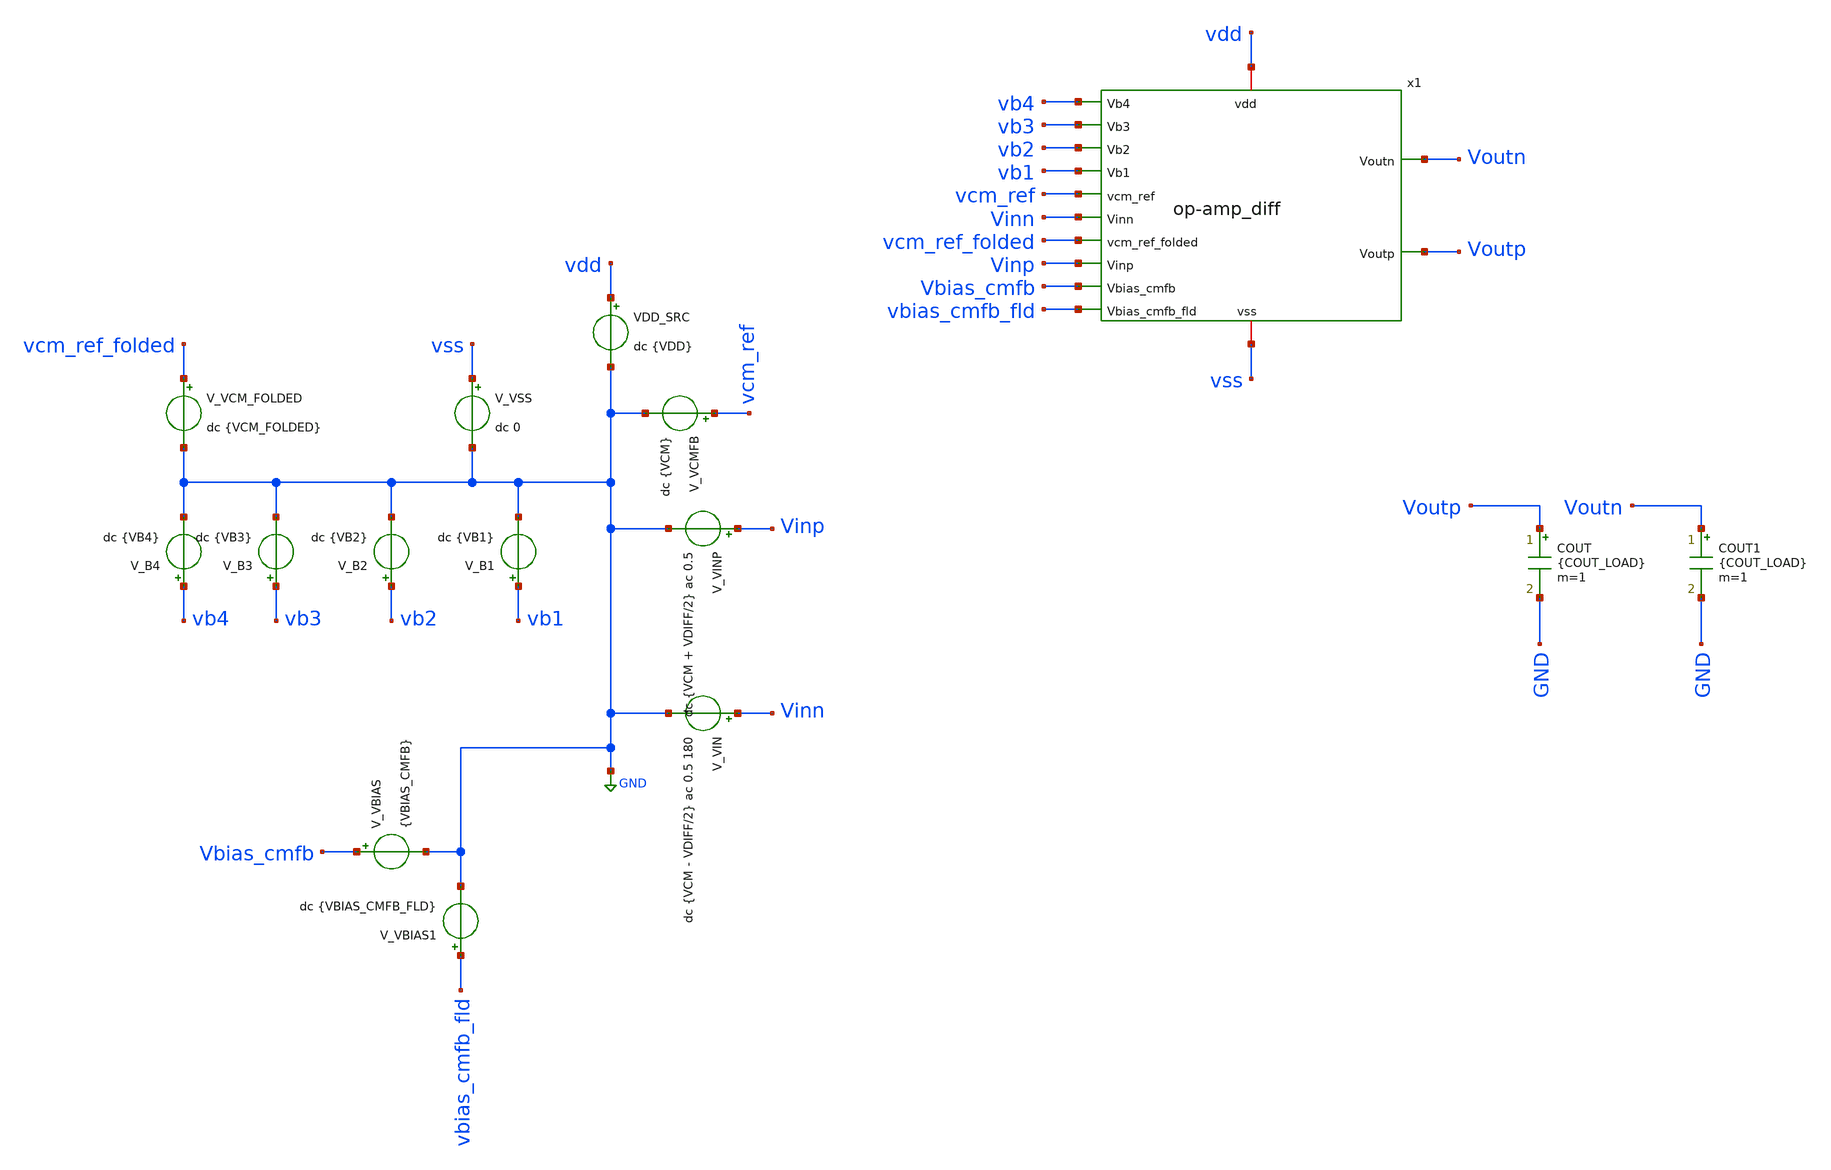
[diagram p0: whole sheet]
** sch_path: circuit_files/sar_adc_test/tb/ota_diff_tb.sch
**.subckt ota_diff_tb
V_VIN Vinn GND dc {VCM - VDIFF/2} ac 0.5 180
VDD_SRC vdd GND dc {VDD}
V_VINP Vinp GND dc {VCM + VDIFF/2} ac 0.5
V_VSS vss GND dc 0
V_VCMFB vcm_ref GND dc {VCM}
V_B1 vb1 GND dc {VB1}
V_B2 vb2 GND dc {VB2}
V_B3 vb3 GND dc {VB3}
V_B4 vb4 GND dc {VB4}
V_VCM_FOLDED vcm_ref_folded GND dc {VCM_FOLDED}
V_VBIAS Vbias_cmfb GND {VBIAS_CMFB}
V_VBIAS1 vbias_cmfb_fld GND dc {VBIAS_CMFB_FLD}
COUT Voutp GND {COUT_LOAD} m=1
COUT1 Voutn GND {COUT_LOAD} m=1
x1 vb4 vb3 vb2 vb1 Voutn vcm_ref Vinn Voutp vcm_ref_folded vdd Vinp vss Vbias_cmfb vbias_cmfb_fld
+ op-amp_diff
**** begin user architecture code

.include /foss/pdks/gf180mcuD/libs.tech/ngspice/design.ngspice

.lib /foss/pdks/gf180mcuD/libs.tech/ngspice/sm141064.ngspice typical
.lib /foss/pdks/gf180mcuD/libs.tech/ngspice/sm141064.ngspice res_typical
.lib /foss/pdks/gf180mcuD/libs.tech/ngspice/sm141064.ngspice moscap_typical
.lib /foss/pdks/gf180mcuD/libs.tech/ngspice/sm141064.ngspice diode_typical
.lib /foss/pdks/gf180mcuD/libs.tech/ngspice/sm141064.ngspice cap_mim
.lib /foss/pdks/gf180mcuD/libs.tech/ngspice/sm141064.ngspice mimcap_typical

.include /foss/pdks/gf180mcuD/libs.ref/gf180mcu_fd_io/spice/gf180mcu_fd_io.spice



.control

set noaskquit
set wr_singlescale
set measdgt=8
set numdgt=8
save all

shell rm -f ota_summary_report.txt
shell rm -f ota_detailed_report.txt
shell rm -f ota_ac_response.txt

echo ================================================== > ota_summary_report.txt
echo FINAL FULLY-DIFFERENTIAL OTA SUMMARY REPORT >> ota_summary_report.txt
echo NMOS-INPUT OTA WITH ACTIVE OUTPUT/FOLDED CMFB >> ota_summary_report.txt
echo ================================================== >> ota_summary_report.txt

echo ================================================== > ota_detailed_report.txt
echo FINAL FULLY-DIFFERENTIAL OTA DETAILED REPORT >> ota_detailed_report.txt
echo NMOS-INPUT OTA WITH ACTIVE OUTPUT/FOLDED CMFB >> ota_detailed_report.txt
echo ================================================== >> ota_detailed_report.txt

echo ---------------- PARAMETERS ---------------- >> ota_summary_report.txt
echo VDD=3.3 VCM=1.65 VDIFF=0 VCM_FOLDED=2.40 >> ota_summary_report.txt
echo VB1=0.58 VB2=2.637 VB3=2.25 VB4=1.15 >> ota_summary_report.txt
echo VBIAS_CMFB=0.82 VBIAS_CMFB_FLD=2.55 >> ota_summary_report.txt
echo Cn=500f Rn=8k COUT_LOAD=200f >> ota_summary_report.txt
echo Active output CMFB: no Rcm resistor network >> ota_summary_report.txt
echo Active folded CMFB: no Rcm_fld resistor network >> ota_summary_report.txt
echo CCMFB=500f CCMFB_FLD=1p >> ota_summary_report.txt
echo -------------------------------------------------- >> ota_summary_report.txt

echo ---------------- PARAMETERS ---------------- >> ota_detailed_report.txt
echo VDD=3.3 VCM=1.65 VDIFF=0 >> ota_detailed_report.txt
echo VCM_FOLDED=2.40 >> ota_detailed_report.txt
echo VB1=0.58 VB2=2.637 VB3=2.25 VB4=1.15 >> ota_detailed_report.txt
echo VBIAS_CMFB=0.82 VBIAS_CMFB_FLD=2.55 >> ota_detailed_report.txt
echo Cn=500f Rn=8k COUT_LOAD=200f >> ota_detailed_report.txt
echo Active output CMFB: no Rcm resistor network >> ota_detailed_report.txt
echo Active folded CMFB: no Rcm_fld resistor network >> ota_detailed_report.txt
echo CCMFB=500f CCMFB_FLD=1p >> ota_detailed_report.txt
echo -------------------------------------------------- >> ota_detailed_report.txt


* ============================================================
* DC OPERATING POINT
* ============================================================

op

let vdd_num          = 3.3

let voutcm_op        = 0.5*(v(voutp)+v(voutn))
let voutdiff_op      = v(voutp)-v(voutn)

let va_cm_op         = 0.5*(v(x1.va)+v(x1.vb))
let vx_cm_op         = 0.5*(v(x1.vx)+v(x1.vy))
let net45_cm_op      = 0.5*(v(x1.net4)+v(x1.net5))

let out_cm_err       = voutcm_op - v(vcm_ref)
let folded_cm_err    = va_cm_op - v(vcm_ref_folded)

let idd_op           = -i(VDD_SRC)
let pdc_op           = vdd_num*idd_op

echo ---------------- OP SUMMARY ---------------- >> ota_summary_report.txt
echo VOUTP VOUTN VOUTCM VOUTDIFF OUT_CM_ERR >> ota_summary_report.txt
echo $&v(voutp) $&v(voutn) $&voutcm_op $&voutdiff_op $&out_cm_err >> ota_summary_report.txt
echo VA VB VA_CM VCM_REF_FOLDED FOLDED_CM_ERR >> ota_summary_report.txt
echo $&v(x1.va) $&v(x1.vb) $&va_cm_op $&v(vcm_ref_folded) $&folded_cm_err >> ota_summary_report.txt
echo VBIAS_OUT VB5 NET8 NET9 IDD PDC >> ota_summary_report.txt
echo $&v(x1.vbias_out) $&v(x1.vb5) $&v(x1.net8) $&v(x1.net9) $&idd_op $&pdc_op >>
+ ota_summary_report.txt
echo -------------------------------------------------- >> ota_summary_report.txt

echo ---------------- OP DETAILED NODES ---------------- >> ota_detailed_report.txt
echo VOUTP=$&v(voutp) >> ota_detailed_report.txt
echo VOUTN=$&v(voutn) >> ota_detailed_report.txt
echo VOUTCM=$&voutcm_op >> ota_detailed_report.txt
echo VOUTDIFF=$&voutdiff_op >> ota_detailed_report.txt
echo VCM_REF_OUTPUT=$&v(vcm_ref) >> ota_detailed_report.txt
echo OUT_CM_ERR=$&out_cm_err >> ota_detailed_report.txt

echo VBIAS_OUT=$&v(x1.vbias_out) >> ota_detailed_report.txt

echo VX=$&v(x1.vx) >> ota_detailed_report.txt
echo VY=$&v(x1.vy) >> ota_detailed_report.txt
echo VX_CM=$&vx_cm_op >> ota_detailed_report.txt

echo VA=$&v(x1.va) >> ota_detailed_report.txt
echo VB=$&v(x1.vb) >> ota_detailed_report.txt
echo VA_CM=$&va_cm_op >> ota_detailed_report.txt
echo VCM_REF_FOLDED=$&v(vcm_ref_folded) >> ota_detailed_report.txt
echo FOLDED_CM_ERR=$&folded_cm_err >> ota_detailed_report.txt

echo NET1=$&v(x1.net1) >> ota_detailed_report.txt
echo NET4=$&v(x1.net4) >> ota_detailed_report.txt
echo NET5=$&v(x1.net5) >> ota_detailed_report.txt
echo NET4_NET5_CM=$&net45_cm_op >> ota_detailed_report.txt

echo VB5=$&v(x1.vb5) >> ota_detailed_report.txt
echo NET8=$&v(x1.net8) >> ota_detailed_report.txt
echo NET9=$&v(x1.net9) >> ota_detailed_report.txt

echo IDD=$&idd_op >> ota_detailed_report.txt
echo PDC=$&pdc_op >> ota_detailed_report.txt
echo -------------------------------------------------- >> ota_detailed_report.txt

print v(voutp) v(voutn) voutcm_op voutdiff_op out_cm_err
print v(x1.vbias_out)
print v(x1.vx) v(x1.vy) vx_cm_op
print v(x1.va) v(x1.vb) va_cm_op folded_cm_err
print v(x1.net1) v(x1.net4) v(x1.net5) net45_cm_op
print v(x1.vb5) v(x1.net8) v(x1.net9)
print idd_op pdc_op


* ============================================================
* DIFFERENTIAL AC ANALYSIS
*
* Input source setup expected:
*   V_VINP Vinp GND dc {VCM + VDIFF/2} ac 0.5
*   V_VIN  Vinn GND dc {VCM - VDIFF/2} ac 0.5 180
*
* This gives vin_diff = Vinp - Vinn = 1 V AC.
* ============================================================

ac dec 200 1 1G

let vin_diff        = v(vinp)-v(vinn)
let vin_cm          = 0.5*(v(vinp)+v(vinn))

let vin_diff_mag    = mag(vin_diff)
let vin_cm_mag      = mag(vin_cm)

let vout_diff       = v(voutp)-v(voutn)
let vout_cm_ac      = 0.5*(v(voutp)+v(voutn))

let vout_diff_mag   = mag(vout_diff)
let vout_cm_mag     = mag(vout_cm_ac)

let avd             = vout_diff/(vin_diff+1e-30)
let avd_mag         = mag(avd)
let avd_db          = 20*log10(avd_mag+1e-30)

let avd_phase_rad   = cph(avd)
let avd_phase_deg   = 57.2957795*avd_phase_rad

let gain_voutp      = v(voutp)/(vin_diff+1e-30)
let gain_voutn      = v(voutn)/(vin_diff+1e-30)
let gain_cmout      = vout_cm_ac/(vin_diff+1e-30)

let gain_voutp_db   = 20*log10(mag(gain_voutp)+1e-30)
let gain_voutn_db   = 20*log10(mag(gain_voutn)+1e-30)
let gain_cmout_db   = 20*log10(mag(gain_cmout)+1e-30)

* Differential-input to output-common-mode leakage.
* This should be as negative as possible.
let cm_leak_ratio   = vout_cm_ac/(vout_diff+1e-30)
let cm_leak_rel_db  = 20*log10(mag(cm_leak_ratio)+1e-30)

* Same information but positive number:
* AVD_DB - GAIN_CMOUT_DB.
let cm_rej_from_diff_db = avd_db - gain_cmout_db

let gain_vxvy       = (v(x1.vx)-v(x1.vy))/(vin_diff+1e-30)
let gain_vavb       = (v(x1.va)-v(x1.vb))/(vin_diff+1e-30)
let gain_stage2     = avd/(gain_vavb+1e-30)

let gain_vxvy_db    = 20*log10(mag(gain_vxvy)+1e-30)
let gain_vavb_db    = 20*log10(mag(gain_vavb)+1e-30)
let gain_stage2_db  = 20*log10(mag(gain_stage2)+1e-30)

let gain_vx_db      = 20*log10(mag(v(x1.vx)/(vin_diff+1e-30))+1e-30)
let gain_vy_db      = 20*log10(mag(v(x1.vy)/(vin_diff+1e-30))+1e-30)
let gain_va_db      = 20*log10(mag(v(x1.va)/(vin_diff+1e-30))+1e-30)
let gain_vb_db      = 20*log10(mag(v(x1.vb)/(vin_diff+1e-30))+1e-30)
let gain_net4_db    = 20*log10(mag(v(x1.net4)/(vin_diff+1e-30))+1e-30)
let gain_net5_db    = 20*log10(mag(v(x1.net5)/(vin_diff+1e-30))+1e-30)


* ============================================================
* LOW-FREQUENCY AC MEASUREMENTS
* ============================================================

meas ac VIN_DIFF_1HZ              find vin_diff_mag          at=1
meas ac VIN_CM_1HZ                find vin_cm_mag            at=1

meas ac VOUT_DIFF_MAG_1HZ         find vout_diff_mag         at=1
meas ac VOUT_CM_MAG_1HZ           find vout_cm_mag           at=1

meas ac AVD_MAG_1HZ               find avd_mag               at=1
meas ac AVD_DB_1HZ                find avd_db                at=1
meas ac AVD_PHASE_1HZ_RAD         find avd_phase_rad         at=1
meas ac AVD_PHASE_1HZ_DEG         find avd_phase_deg         at=1

meas ac GAIN_VOUTP_DB_1HZ         find gain_voutp_db         at=1
meas ac GAIN_VOUTN_DB_1HZ         find gain_voutn_db         at=1
meas ac GAIN_CMOUT_DB_1HZ         find gain_cmout_db         at=1

meas ac CM_LEAK_REL_DB_1HZ        find cm_leak_rel_db        at=1
meas ac CM_REJ_FROM_DIFF_DB_1HZ   find cm_rej_from_diff_db   at=1

meas ac GAIN_VX_DB_1HZ            find gain_vx_db            at=1
meas ac GAIN_VY_DB_1HZ            find gain_vy_db            at=1
meas ac GAIN_VA_DB_1HZ            find gain_va_db            at=1
meas ac GAIN_VB_DB_1HZ            find gain_vb_db            at=1
meas ac GAIN_NET4_DB_1HZ          find gain_net4_db          at=1
meas ac GAIN_NET5_DB_1HZ          find gain_net5_db          at=1

meas ac GAIN_VXVY_DB_1HZ          find gain_vxvy_db          at=1
meas ac GAIN_VAVB_DB_1HZ          find gain_vavb_db          at=1
meas ac GAIN_STAGE2_DB_1HZ        find gain_stage2_db        at=1


* ============================================================
* BANDWIDTH, UGF, PHASE MARGIN
* ============================================================

let avd_3db_target = avd_db_1hz - 3

meas ac FP_DOM                when avd_db=avd_3db_target fall=1
meas ac UGF                   when avd_db=0 fall=1
meas ac PHASE_AT_UGF_RAD      find avd_phase_rad when avd_db=0 fall=1
meas ac PHASE_AT_UGF_DEG      find avd_phase_deg when avd_db=0 fall=1

let phase_at_ugf_deg_wrapped = phase_at_ugf_deg

while phase_at_ugf_deg_wrapped < -180
  let phase_at_ugf_deg_wrapped = phase_at_ugf_deg_wrapped + 360
end

while phase_at_ugf_deg_wrapped > 180
  let phase_at_ugf_deg_wrapped = phase_at_ugf_deg_wrapped - 360
end

let PM_EST = 180 + phase_at_ugf_deg_wrapped


* ============================================================
* SPOT CHECKS
* ============================================================

meas ac AVD_DB_10K              find avd_db              at=10k
meas ac AVD_DB_100K             find avd_db              at=100k
meas ac AVD_DB_1MEG             find avd_db              at=1Meg
meas ac AVD_DB_10MEG            find avd_db              at=10Meg
meas ac AVD_DB_100MEG           find avd_db              at=100Meg

meas ac PHASE_10K_DEG           find avd_phase_deg       at=10k
meas ac PHASE_100K_DEG          find avd_phase_deg       at=100k
meas ac PHASE_1MEG_DEG          find avd_phase_deg       at=1Meg
meas ac PHASE_10MEG_DEG         find avd_phase_deg       at=10Meg
meas ac PHASE_100MEG_DEG        find avd_phase_deg       at=100Meg

meas ac GAIN_CMOUT_DB_10K       find gain_cmout_db       at=10k
meas ac GAIN_CMOUT_DB_100K      find gain_cmout_db       at=100k
meas ac GAIN_CMOUT_DB_1MEG      find gain_cmout_db       at=1Meg

meas ac CM_LEAK_REL_DB_10K      find cm_leak_rel_db      at=10k
meas ac CM_LEAK_REL_DB_100K     find cm_leak_rel_db      at=100k
meas ac CM_LEAK_REL_DB_1MEG     find cm_leak_rel_db      at=1Meg


* ============================================================
* WRITE SUMMARY REPORT
* ============================================================

echo ---------------- AC SUMMARY ---------------- >> ota_summary_report.txt
echo VIN_DIFF_1HZ=$&vin_diff_1hz >> ota_summary_report.txt
echo VIN_CM_1HZ=$&vin_cm_1hz >> ota_summary_report.txt
echo VOUT_DIFF_MAG_1HZ=$&vout_diff_mag_1hz >> ota_summary_report.txt
echo VOUT_CM_MAG_1HZ=$&vout_cm_mag_1hz >> ota_summary_report.txt

echo DC_DIFF_GAIN_LINEAR=$&avd_mag_1hz >> ota_summary_report.txt
echo DC_DIFF_GAIN_DB=$&avd_db_1hz >> ota_summary_report.txt
echo DC_PHASE_1HZ_DEG=$&avd_phase_1hz_deg >> ota_summary_report.txt

echo OUTPUT_CM_GAIN_FROM_DIFF_DB_1HZ=$&gain_cmout_db_1hz >> ota_summary_report.txt
echo OUTPUT_CM_LEAK_REL_TO_DIFF_DB_1HZ=$&cm_leak_rel_db_1hz >> ota_summary_report.txt
echo OUTPUT_CM_REJECTION_FROM_DIFF_DB_1HZ=$&cm_rej_from_diff_db_1hz >> ota_summary_report.txt

echo STAGE1_GAIN_VAVB_DB=$&gain_vavb_db_1hz >> ota_summary_report.txt
echo STAGE2_GAIN_EST_DB=$&gain_stage2_db_1hz >> ota_summary_report.txt

echo DOMINANT_POLE_HZ=$&fp_dom >> ota_summary_report.txt
echo UNITY_GAIN_FREQ_HZ=$&ugf >> ota_summary_report.txt
echo PHASE_AT_UGF_RAW_DEG=$&phase_at_ugf_deg >> ota_summary_report.txt
echo PHASE_AT_UGF_WRAPPED_DEG=$&phase_at_ugf_deg_wrapped >> ota_summary_report.txt
echo PHASE_MARGIN_EST_DEG=$&PM_EST >> ota_summary_report.txt
echo -------------------------------------------------- >> ota_summary_report.txt

echo ---------------- PASS TARGETS TO CHECK ---------------- >> ota_summary_report.txt
echo DC output CM: VOUTCM should be near 1.65 V >> ota_summary_report.txt
echo DC folded CM: VA_CM should be near 2.40 V >> ota_summary_report.txt
echo IDD target: roughly 100 uA to 300 uA is reasonable >> ota_summary_report.txt
echo Differential gain target: AVD_DB should be greater than 75 dB before layout >>
+ ota_summary_report.txt
echo Differential PM target: PM_EST should be greater than 60 deg >> ota_summary_report.txt
echo Output CM leakage target: CM_LEAK_REL_DB should be very negative, preferably below -50 dB >>
+ ota_summary_report.txt
echo Note: active MOS CMFB can create differential-to-common-mode leakage, so check this value
+ carefully. >> ota_summary_report.txt
echo ================================================== >> ota_summary_report.txt


* ============================================================
* WRITE DETAILED REPORT
* ============================================================

echo ---------------- AC DETAILED LOW-FREQUENCY GAINS ---------------- >> ota_detailed_report.txt
echo VIN_DIFF_1HZ=$&vin_diff_1hz >> ota_detailed_report.txt
echo VIN_CM_1HZ=$&vin_cm_1hz >> ota_detailed_report.txt

echo VOUT_DIFF_MAG_1HZ=$&vout_diff_mag_1hz >> ota_detailed_report.txt
echo VOUT_CM_MAG_1HZ=$&vout_cm_mag_1hz >> ota_detailed_report.txt

echo AVD_MAG_1HZ=$&avd_mag_1hz >> ota_detailed_report.txt
echo AVD_DB_1HZ=$&avd_db_1hz >> ota_detailed_report.txt
echo AVD_PHASE_1HZ_RAD=$&avd_phase_1hz_rad >> ota_detailed_report.txt
echo AVD_PHASE_1HZ_DEG=$&avd_phase_1hz_deg >> ota_detailed_report.txt

echo GAIN_VOUTP_DB_1HZ=$&gain_voutp_db_1hz >> ota_detailed_report.txt
echo GAIN_VOUTN_DB_1HZ=$&gain_voutn_db_1hz >> ota_detailed_report.txt
echo GAIN_CMOUT_DB_1HZ=$&gain_cmout_db_1hz >> ota_detailed_report.txt
echo CM_LEAK_REL_DB_1HZ=$&cm_leak_rel_db_1hz >> ota_detailed_report.txt
echo CM_REJ_FROM_DIFF_DB_1HZ=$&cm_rej_from_diff_db_1hz >> ota_detailed_report.txt

echo GAIN_VX_DB_1HZ=$&gain_vx_db_1hz >> ota_detailed_report.txt
echo GAIN_VY_DB_1HZ=$&gain_vy_db_1hz >> ota_detailed_report.txt
echo GAIN_VA_DB_1HZ=$&gain_va_db_1hz >> ota_detailed_report.txt
echo GAIN_VB_DB_1HZ=$&gain_vb_db_1hz >> ota_detailed_report.txt
echo GAIN_NET4_DB_1HZ=$&gain_net4_db_1hz >> ota_detailed_report.txt
echo GAIN_NET5_DB_1HZ=$&gain_net5_db_1hz >> ota_detailed_report.txt

echo GAIN_VXVY_DB_1HZ=$&gain_vxvy_db_1hz >> ota_detailed_report.txt
echo GAIN_VAVB_DB_1HZ=$&gain_vavb_db_1hz >> ota_detailed_report.txt
echo GAIN_STAGE2_DB_1HZ=$&gain_stage2_db_1hz >> ota_detailed_report.txt
echo -------------------------------------------------- >> ota_detailed_report.txt

echo ---------------- AC BANDWIDTH AND PHASE ---------------- >> ota_detailed_report.txt
echo AVD_3DB_TARGET=$&avd_3db_target >> ota_detailed_report.txt
echo FP_DOM_HZ=$&fp_dom >> ota_detailed_report.txt
echo UGF_HZ=$&ugf >> ota_detailed_report.txt
echo PHASE_AT_UGF_RAD=$&phase_at_ugf_rad >> ota_detailed_report.txt
echo PHASE_AT_UGF_RAW_DEG=$&phase_at_ugf_deg >> ota_detailed_report.txt
echo PHASE_AT_UGF_WRAPPED_DEG=$&phase_at_ugf_deg_wrapped >> ota_detailed_report.txt
echo PHASE_MARGIN_EST_DEG=$&PM_EST >> ota_detailed_report.txt

echo AVD_DB_10K=$&avd_db_10k PHASE_10K_DEG=$&phase_10k_deg >> ota_detailed_report.txt
echo AVD_DB_100K=$&avd_db_100k PHASE_100K_DEG=$&phase_100k_deg >> ota_detailed_report.txt
echo AVD_DB_1MEG=$&avd_db_1meg PHASE_1MEG_DEG=$&phase_1meg_deg >> ota_detailed_report.txt
echo AVD_DB_10MEG=$&avd_db_10meg PHASE_10MEG_DEG=$&phase_10meg_deg >> ota_detailed_report.txt
echo AVD_DB_100MEG=$&avd_db_100meg PHASE_100MEG_DEG=$&phase_100meg_deg >> ota_detailed_report.txt

echo GAIN_CMOUT_DB_10K=$&gain_cmout_db_10k CM_LEAK_REL_DB_10K=$&cm_leak_rel_db_10k >>
+ ota_detailed_report.txt
echo GAIN_CMOUT_DB_100K=$&gain_cmout_db_100k CM_LEAK_REL_DB_100K=$&cm_leak_rel_db_100k >>
+ ota_detailed_report.txt
echo GAIN_CMOUT_DB_1MEG=$&gain_cmout_db_1meg CM_LEAK_REL_DB_1MEG=$&cm_leak_rel_db_1meg >>
+ ota_detailed_report.txt
echo -------------------------------------------------- >> ota_detailed_report.txt

echo ---------------- INTERPRETATION NOTES ---------------- >> ota_detailed_report.txt
echo 1. VOUTCM should be near vcm_ref = 1.65 V. >> ota_detailed_report.txt
echo 2. VA_CM should be near vcm_ref_folded = 2.40 V. >> ota_detailed_report.txt
echo 3. VBIAS_OUT around 0.6 to 1.2 V is usually reasonable here. >> ota_detailed_report.txt
echo 4. VB5 around 0.5 to 0.9 V is usually reasonable here. >> ota_detailed_report.txt
echo 5. IDD should remain around hundreds of uA, not mA. >> ota_detailed_report.txt
echo 6. CM_LEAK_REL_DB is output common-mode divided by differential output under differential
+ drive. More negative is better. >> ota_detailed_report.txt
echo 7. This is pre-layout. Recheck after corners, mismatch, PEX, and CMFB loop-gain tests. >>
+ ota_detailed_report.txt
echo ================================================== >> ota_detailed_report.txt


* ============================================================
* SAVE FULL AC TABLE
* ============================================================

wrdata ota_ac_response.txt avd_db avd_phase_deg gain_vavb_db gain_stage2_db gain_cmout_db
+ cm_leak_rel_db cm_rej_from_diff_db gain_voutp_db gain_voutn_db


* ============================================================
* PRINT IMPORTANT VALUES TO TERMINAL
* ============================================================

print avd_mag_1hz avd_db_1hz gain_vavb_db_1hz gain_stage2_db_1hz
print vout_diff_mag_1hz vout_cm_mag_1hz gain_cmout_db_1hz cm_leak_rel_db_1hz cm_rej_from_diff_db_1hz
print fp_dom ugf phase_at_ugf_deg phase_at_ugf_deg_wrapped PM_EST
print avd_db_10k avd_db_100k avd_db_1meg avd_db_10meg avd_db_100meg
print gain_cmout_db_10k gain_cmout_db_100k gain_cmout_db_1meg
print cm_leak_rel_db_10k cm_leak_rel_db_100k cm_leak_rel_db_1meg

echo ==================================================
echo Done.
echo Generated:
echo   ota_summary_report.txt
echo   ota_detailed_report.txt
echo   ota_ac_response.txt
echo ==================================================

.endc





**** begin user architecture code

.param sw_stat_mismatch=0
.param mis_vth=0
.param mis_k=0

.param VDD=3.3
.param VCM=1.65
.param VCM_FOLDED=2.40
.param VDIFF=0

* ============================================================
* Final selected OTA bias
* ============================================================
.param VB1=0.58
.param VB2=2.637
.param VB3=2.25
.param VB4=1.15

.param VBIAS_CMFB=0.82
.param VBIAS_CMFB_FLD=2.55

* ============================================================
* Compensation / load
* ============================================================
.param Cn=500f
.param Rn=8k
.param COUT_LOAD=200f


.param CCMFB=500f
.param CCMFB_FLD=1p

.options reltol=1e-4 abstol=1e-12 vntol=1e-6
.options gmin=1e-12
.options plotwinsize=0
.options method=gear maxord=2

* ============================================================
* Operating-point hints only. These do not force final OP.
* Internal OTA nodes are now inside instance x1.
* ============================================================
.nodeset V(voutp)=1.643
.nodeset V(voutn)=1.643

.nodeset V(x1.vbias_out)=0.866

.nodeset V(x1.vx)=3.022
.nodeset V(x1.vy)=3.022
.nodeset V(x1.va)=2.401
.nodeset V(x1.vb)=2.401

.nodeset V(x1.net1)=0.887
.nodeset V(x1.net4)=0.426
.nodeset V(x1.net5)=0.426

.nodeset V(x1.vb5)=0.713
.nodeset V(x1.net8)=0.578
.nodeset V(x1.net9)=2.624



**** end user architecture code
**.ends

* expanding   symbol:  /media/sf_LNA_chipathon/sar_adc_gf180/xschem/op-amp_diff.sym # of pins=14
** sym_path: circuit_files/sar_adc_test/xschem/op-amp_diff.sym
** sch_path: circuit_files/sar_adc_test/xschem/op-amp_diff.sch
.subckt op-amp_diff Vb4 Vb3 Vb2 Vb1 Voutn vcm_ref Vinn Voutp vcm_ref_folded vdd Vinp vss Vbias_cmfb
+ Vbias_cmfb_fld
*.ipin Vinn
*.opin Voutp
*.iopin vdd
*.ipin Vinp
*.ipin Vb1
*.ipin Vbias_cmfb_fld
*.iopin vss
*.opin Voutn
*.ipin Vbias_cmfb
*.ipin Vb2
*.ipin Vb3
*.ipin Vb4
*.ipin vcm_ref_folded
*.ipin vcm_ref
XM1 Vy Vinn net1 vss nfet_03v3 L=0.5u W=20u nf=1 ad='int((nf+1)/2) * W/nf * 0.18u' as='int((nf+2)/2) * W/nf * 0.18u'
+ pd='2*int((nf+1)/2) * (W/nf + 0.18u)' ps='2*int((nf+2)/2) * (W/nf + 0.18u)' nrd='0.18u / W' nrs='0.18u / W'
+ sa=0 sb=0 sd=0 m=1
XM4 net1 Vb1 vss vss nfet_03v3 L=1u W=10u nf=1 ad='int((nf+1)/2) * W/nf * 0.18u' as='int((nf+2)/2) * W/nf * 0.18u'
+ pd='2*int((nf+1)/2) * (W/nf + 0.18u)' ps='2*int((nf+2)/2) * (W/nf + 0.18u)' nrd='0.18u / W' nrs='0.18u / W'
+ sa=0 sb=0 sd=0 m=1
XM3 Vx Vinp net1 vss nfet_03v3 L=0.5u W=20u nf=1 ad='int((nf+1)/2) * W/nf * 0.18u' as='int((nf+2)/2) * W/nf * 0.18u'
+ pd='2*int((nf+1)/2) * (W/nf + 0.18u)' ps='2*int((nf+2)/2) * (W/nf + 0.18u)' nrd='0.18u / W' nrs='0.18u / W'
+ sa=0 sb=0 sd=0 m=1
XM7 Voutp Vbias_out vss vss nfet_03v3 L=1u W=30u nf=1 ad='int((nf+1)/2) * W/nf * 0.18u' as='int((nf+2)/2) * W/nf * 0.18u'
+ pd='2*int((nf+1)/2) * (W/nf + 0.18u)' ps='2*int((nf+2)/2) * (W/nf + 0.18u)' nrd='0.18u / W' nrs='0.18u / W'
+ sa=0 sb=0 sd=0 m=1
XM8 Voutp Vb vdd vdd pfet_03v3 L=0.5u W=40u nf=1 ad='int((nf+1)/2) * W/nf * 0.18u' as='int((nf+2)/2) * W/nf * 0.18u'
+ pd='2*int((nf+1)/2) * (W/nf + 0.18u)' ps='2*int((nf+2)/2) * (W/nf + 0.18u)' nrd='0.18u / W' nrs='0.18u / W'
+ sa=0 sb=0 sd=0 m=3
XM6 Voutn Vbias_out vss vss nfet_03v3 L=1u W=30u nf=1 ad='int((nf+1)/2) * W/nf * 0.18u' as='int((nf+2)/2) * W/nf * 0.18u'
+ pd='2*int((nf+1)/2) * (W/nf + 0.18u)' ps='2*int((nf+2)/2) * (W/nf + 0.18u)' nrd='0.18u / W' nrs='0.18u / W'
+ sa=0 sb=0 sd=0 m=1
XM9 Voutn Va vdd vdd pfet_03v3 L=0.5u W=40u nf=1 ad='int((nf+1)/2) * W/nf * 0.18u' as='int((nf+2)/2) * W/nf * 0.18u'
+ pd='2*int((nf+1)/2) * (W/nf + 0.18u)' ps='2*int((nf+2)/2) * (W/nf + 0.18u)' nrd='0.18u / W' nrs='0.18u / W'
+ sa=0 sb=0 sd=0 m=3
XM10 Vy Vb2 vdd vdd pfet_03v3 L=0.5u W=40u nf=1 ad='int((nf+1)/2) * W/nf * 0.18u' as='int((nf+2)/2) * W/nf * 0.18u'
+ pd='2*int((nf+1)/2) * (W/nf + 0.18u)' ps='2*int((nf+2)/2) * (W/nf + 0.18u)' nrd='0.18u / W' nrs='0.18u / W'
+ sa=0 sb=0 sd=0 m=3
XM11 Vx Vb2 vdd vdd pfet_03v3 L=0.5u W=40u nf=1 ad='int((nf+1)/2) * W/nf * 0.18u' as='int((nf+2)/2) * W/nf * 0.18u'
+ pd='2*int((nf+1)/2) * (W/nf + 0.18u)' ps='2*int((nf+2)/2) * (W/nf + 0.18u)' nrd='0.18u / W' nrs='0.18u / W'
+ sa=0 sb=0 sd=0 m=3
XM12 Va Vb3 Vy vdd pfet_03v3 L=0.5u W=40u nf=1 ad='int((nf+1)/2) * W/nf * 0.18u' as='int((nf+2)/2) * W/nf * 0.18u'
+ pd='2*int((nf+1)/2) * (W/nf + 0.18u)' ps='2*int((nf+2)/2) * (W/nf + 0.18u)' nrd='0.18u / W' nrs='0.18u / W'
+ sa=0 sb=0 sd=0 m=3
XM13 Vb Vb3 Vx vdd pfet_03v3 L=0.5u W=40u nf=1 ad='int((nf+1)/2) * W/nf * 0.18u' as='int((nf+2)/2) * W/nf * 0.18u'
+ pd='2*int((nf+1)/2) * (W/nf + 0.18u)' ps='2*int((nf+2)/2) * (W/nf + 0.18u)' nrd='0.18u / W' nrs='0.18u / W'
+ sa=0 sb=0 sd=0 m=3
XM14 Vb Vb4 net5 vss nfet_03v3 L=1u W=30u nf=1 ad='int((nf+1)/2) * W/nf * 0.18u' as='int((nf+2)/2) * W/nf * 0.18u'
+ pd='2*int((nf+1)/2) * (W/nf + 0.18u)' ps='2*int((nf+2)/2) * (W/nf + 0.18u)' nrd='0.18u / W' nrs='0.18u / W'
+ sa=0 sb=0 sd=0 m=1
XM15 Va Vb4 net4 vss nfet_03v3 L=1u W=30u nf=1 ad='int((nf+1)/2) * W/nf * 0.18u' as='int((nf+2)/2) * W/nf * 0.18u'
+ pd='2*int((nf+1)/2) * (W/nf + 0.18u)' ps='2*int((nf+2)/2) * (W/nf + 0.18u)' nrd='0.18u / W' nrs='0.18u / W'
+ sa=0 sb=0 sd=0 m=1
XM16 net5 Vb5 vss vss nfet_03v3 L=1u W=2u nf=1 ad='int((nf+1)/2) * W/nf * 0.18u' as='int((nf+2)/2) * W/nf * 0.18u'
+ pd='2*int((nf+1)/2) * (W/nf + 0.18u)' ps='2*int((nf+2)/2) * (W/nf + 0.18u)' nrd='0.18u / W' nrs='0.18u / W'
+ sa=0 sb=0 sd=0 m=1
XM17 net4 Vb5 vss vss nfet_03v3 L=1u W=2u nf=1 ad='int((nf+1)/2) * W/nf * 0.18u' as='int((nf+2)/2) * W/nf * 0.18u'
+ pd='2*int((nf+1)/2) * (W/nf + 0.18u)' ps='2*int((nf+2)/2) * (W/nf + 0.18u)' nrd='0.18u / W' nrs='0.18u / W'
+ sa=0 sb=0 sd=0 m=1
C3 Voutn net3 {Cn} m=1
R3 Va net3 {Rn} m=1
R1 Vb net2 {Rn} m=1
C1 net2 Voutp {Cn} m=1
C2 Vbias_out vss {CCMFB} m=1
XM2 net7 Voutn net6 vss nfet_03v3 L=3u W=1u nf=2 ad='int((nf+1)/2) * W/nf * 0.18u' as='int((nf+2)/2) * W/nf * 0.18u'
+ pd='2*int((nf+1)/2) * (W/nf + 0.18u)' ps='2*int((nf+2)/2) * (W/nf + 0.18u)' nrd='0.18u / W' nrs='0.18u / W'
+ sa=0 sb=0 sd=0 m=1
XM5 net6 Vbias_cmfb vss vss nfet_03v3 L=1u W=5u nf=1 ad='int((nf+1)/2) * W/nf * 0.18u' as='int((nf+2)/2) * W/nf * 0.18u'
+ pd='2*int((nf+1)/2) * (W/nf + 0.18u)' ps='2*int((nf+2)/2) * (W/nf + 0.18u)' nrd='0.18u / W' nrs='0.18u / W'
+ sa=0 sb=0 sd=0 m=1
XM18 Vbias_out net7 vdd vdd pfet_03v3 L=1u W=20u nf=2 ad='int((nf+1)/2) * W/nf * 0.18u' as='int((nf+2)/2) * W/nf * 0.18u'
+ pd='2*int((nf+1)/2) * (W/nf + 0.18u)' ps='2*int((nf+2)/2) * (W/nf + 0.18u)' nrd='0.18u / W' nrs='0.18u / W'
+ sa=0 sb=0 sd=0 m=1
XM19 Vbias_out vcm_ref net6 vss nfet_03v3 L=3u W=1u nf=2 ad='int((nf+1)/2) * W/nf * 0.18u' as='int((nf+2)/2) * W/nf * 0.18u'
+ pd='2*int((nf+1)/2) * (W/nf + 0.18u)' ps='2*int((nf+2)/2) * (W/nf + 0.18u)' nrd='0.18u / W' nrs='0.18u / W'
+ sa=0 sb=0 sd=0 m=1
XM21 net7 net7 vdd vdd pfet_03v3 L=1u W=20u nf=2 ad='int((nf+1)/2) * W/nf * 0.18u' as='int((nf+2)/2) * W/nf * 0.18u'
+ pd='2*int((nf+1)/2) * (W/nf + 0.18u)' ps='2*int((nf+2)/2) * (W/nf + 0.18u)' nrd='0.18u / W' nrs='0.18u / W'
+ sa=0 sb=0 sd=0 m=1
C4 Vb5 vss {CCMFB_FLD} m=1
XM20 net8 Vb net9 vdd pfet_03v3 L=1u W=5u nf=1 ad='int((nf+1)/2) * W/nf * 0.18u' as='int((nf+2)/2) * W/nf * 0.18u'
+ pd='2*int((nf+1)/2) * (W/nf + 0.18u)' ps='2*int((nf+2)/2) * (W/nf + 0.18u)' nrd='0.18u / W' nrs='0.18u / W'
+ sa=0 sb=0 sd=0 m=1
XM24 Vb5 vcm_ref_folded net9 vdd pfet_03v3 L=1u W=5u nf=1 ad='int((nf+1)/2) * W/nf * 0.18u' as='int((nf+2)/2) * W/nf * 0.18u'
+ pd='2*int((nf+1)/2) * (W/nf + 0.18u)' ps='2*int((nf+2)/2) * (W/nf + 0.18u)' nrd='0.18u / W' nrs='0.18u / W'
+ sa=0 sb=0 sd=0 m=1
XM22 net8 net8 vss vss nfet_03v3 L=1u W=10u nf=1 ad='int((nf+1)/2) * W/nf * 0.18u' as='int((nf+2)/2) * W/nf * 0.18u'
+ pd='2*int((nf+1)/2) * (W/nf + 0.18u)' ps='2*int((nf+2)/2) * (W/nf + 0.18u)' nrd='0.18u / W' nrs='0.18u / W'
+ sa=0 sb=0 sd=0 m=1
XM23 Vb5 net8 vss vss nfet_03v3 L=1u W=10u nf=1 ad='int((nf+1)/2) * W/nf * 0.18u' as='int((nf+2)/2) * W/nf * 0.18u'
+ pd='2*int((nf+1)/2) * (W/nf + 0.18u)' ps='2*int((nf+2)/2) * (W/nf + 0.18u)' nrd='0.18u / W' nrs='0.18u / W'
+ sa=0 sb=0 sd=0 m=1
XM25 net9 Vbias_cmfb_fld vdd vdd pfet_03v3 L=1u W=20u nf=2 ad='int((nf+1)/2) * W/nf * 0.18u' as='int((nf+2)/2) * W/nf * 0.18u'
+ pd='2*int((nf+1)/2) * (W/nf + 0.18u)' ps='2*int((nf+2)/2) * (W/nf + 0.18u)' nrd='0.18u / W' nrs='0.18u / W'
+ sa=0 sb=0 sd=0 m=1
XM26 net8 Va net9 vdd pfet_03v3 L=1u W=5u nf=1 ad='int((nf+1)/2) * W/nf * 0.18u' as='int((nf+2)/2) * W/nf * 0.18u'
+ pd='2*int((nf+1)/2) * (W/nf + 0.18u)' ps='2*int((nf+2)/2) * (W/nf + 0.18u)' nrd='0.18u / W' nrs='0.18u / W'
+ sa=0 sb=0 sd=0 m=1
XM28 Vb5 vcm_ref_folded net9 vdd pfet_03v3 L=1u W=5u nf=1 ad='int((nf+1)/2) * W/nf * 0.18u' as='int((nf+2)/2) * W/nf * 0.18u'
+ pd='2*int((nf+1)/2) * (W/nf + 0.18u)' ps='2*int((nf+2)/2) * (W/nf + 0.18u)' nrd='0.18u / W' nrs='0.18u / W'
+ sa=0 sb=0 sd=0 m=1
XM27 net7 Voutp net6 vss nfet_03v3 L=3u W=1u nf=2 ad='int((nf+1)/2) * W/nf * 0.18u' as='int((nf+2)/2) * W/nf * 0.18u'
+ pd='2*int((nf+1)/2) * (W/nf + 0.18u)' ps='2*int((nf+2)/2) * (W/nf + 0.18u)' nrd='0.18u / W' nrs='0.18u / W'
+ sa=0 sb=0 sd=0 m=1
XM29 Vbias_out vcm_ref net6 vss nfet_03v3 L=3u W=1u nf=2 ad='int((nf+1)/2) * W/nf * 0.18u' as='int((nf+2)/2) * W/nf * 0.18u'
+ pd='2*int((nf+1)/2) * (W/nf + 0.18u)' ps='2*int((nf+2)/2) * (W/nf + 0.18u)' nrd='0.18u / W' nrs='0.18u / W'
+ sa=0 sb=0 sd=0 m=1
.ends

.GLOBAL GND
.end
